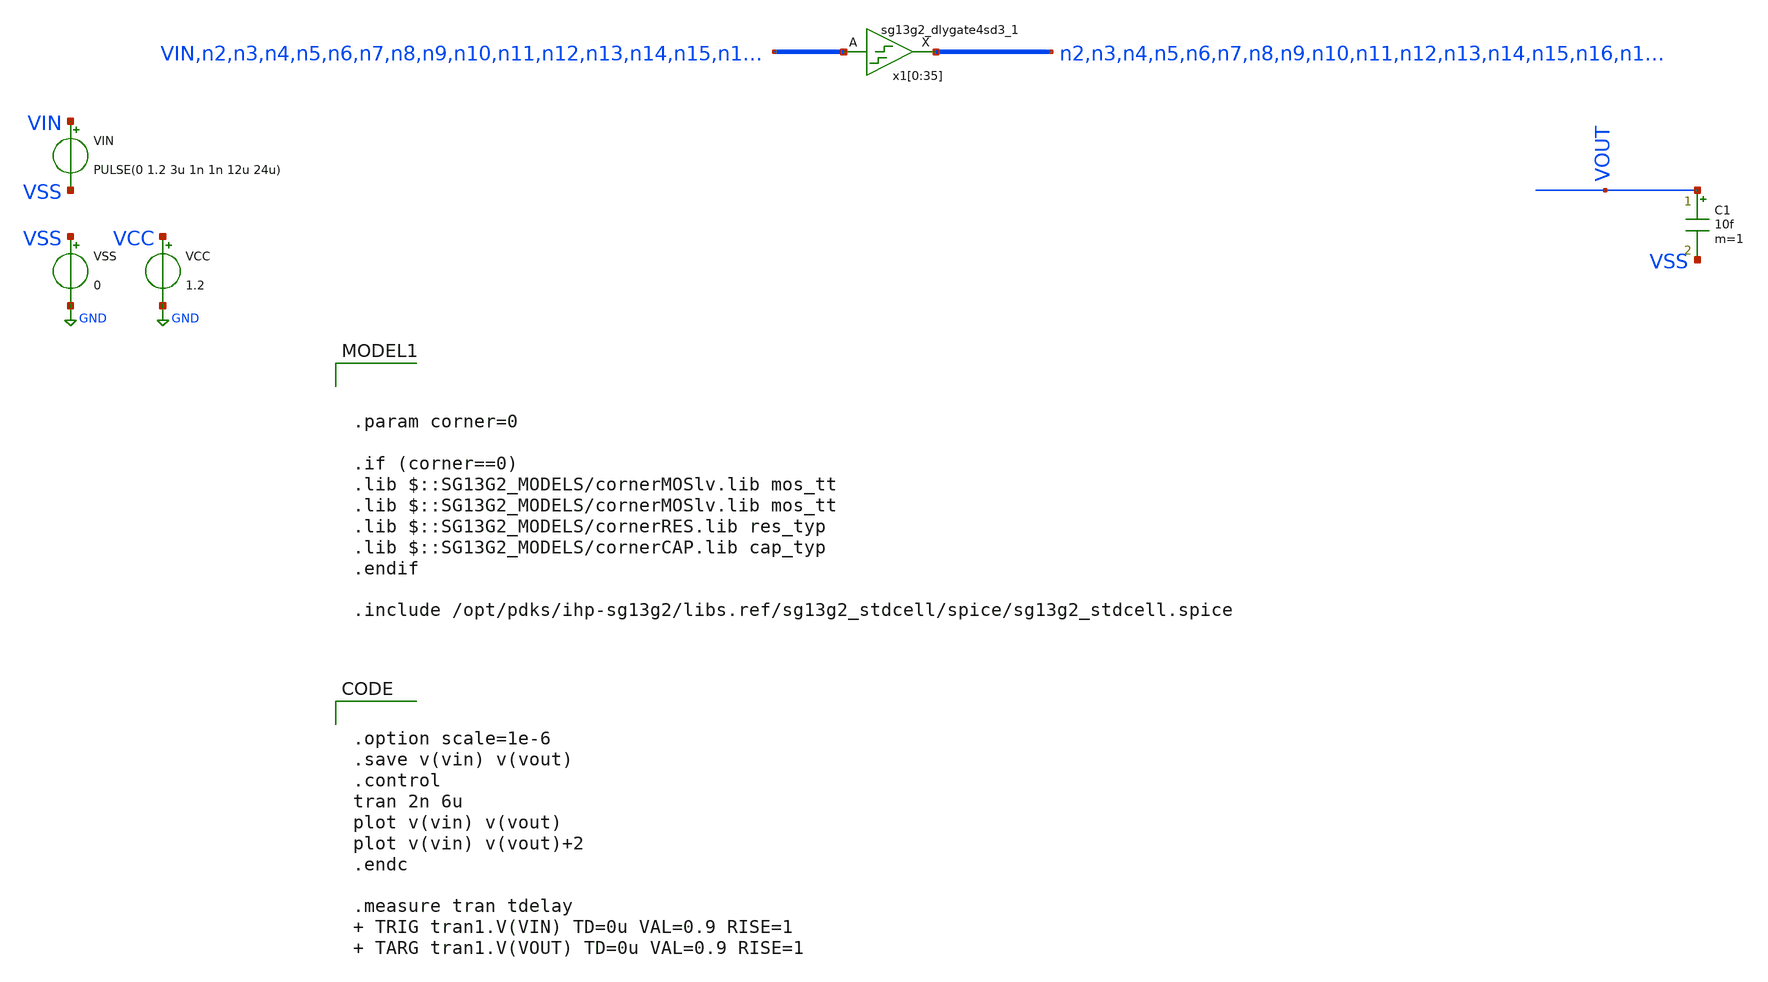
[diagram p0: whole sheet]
** sch_path: xschem/tb_largedelay_reportslack.sch
**.subckt tb_largedelay_reportslack
VCC VCC GND 1.2
VSS VSS GND 0
VIN VIN VSS PULSE(0 1.2 3u 1n 1n 12u 24u)
C1 VOUT VSS 10f m=1
x1[0] n2 VIN VCC VSS sg13g2_dlygate4sd3_1
x1[1] n3 n2 VCC VSS sg13g2_dlygate4sd3_1
x1[2] n4 n3 VCC VSS sg13g2_dlygate4sd3_1
x1[3] n5 n4 VCC VSS sg13g2_dlygate4sd3_1
x1[4] n6 n5 VCC VSS sg13g2_dlygate4sd3_1
x1[5] n7 n6 VCC VSS sg13g2_dlygate4sd3_1
x1[6] n8 n7 VCC VSS sg13g2_dlygate4sd3_1
x1[7] n9 n8 VCC VSS sg13g2_dlygate4sd3_1
x1[8] n10 n9 VCC VSS sg13g2_dlygate4sd3_1
x1[9] n11 n10 VCC VSS sg13g2_dlygate4sd3_1
x1[10] n12 n11 VCC VSS sg13g2_dlygate4sd3_1
x1[11] n13 n12 VCC VSS sg13g2_dlygate4sd3_1
x1[12] n14 n13 VCC VSS sg13g2_dlygate4sd3_1
x1[13] n15 n14 VCC VSS sg13g2_dlygate4sd3_1
x1[14] n16 n15 VCC VSS sg13g2_dlygate4sd3_1
x1[15] n17 n16 VCC VSS sg13g2_dlygate4sd3_1
x1[16] n18 n17 VCC VSS sg13g2_dlygate4sd3_1
x1[17] n19 n18 VCC VSS sg13g2_dlygate4sd3_1
x1[18] n20 n19 VCC VSS sg13g2_dlygate4sd3_1
x1[19] n21 n20 VCC VSS sg13g2_dlygate4sd3_1
x1[20] n22 n21 VCC VSS sg13g2_dlygate4sd3_1
x1[21] n23 n22 VCC VSS sg13g2_dlygate4sd3_1
x1[22] n24 n23 VCC VSS sg13g2_dlygate4sd3_1
x1[23] n25 n24 VCC VSS sg13g2_dlygate4sd3_1
x1[24] n26 n25 VCC VSS sg13g2_dlygate4sd3_1
x1[25] n27 n26 VCC VSS sg13g2_dlygate4sd3_1
x1[26] n28 n27 VCC VSS sg13g2_dlygate4sd3_1
x1[27] n29 n28 VCC VSS sg13g2_dlygate4sd3_1
x1[28] n30 n29 VCC VSS sg13g2_dlygate4sd3_1
x1[29] n31 n30 VCC VSS sg13g2_dlygate4sd3_1
x1[30] n32 n31 VCC VSS sg13g2_dlygate4sd3_1
x1[31] n33 n32 VCC VSS sg13g2_dlygate4sd3_1
x1[32] n34 n33 VCC VSS sg13g2_dlygate4sd3_1
x1[33] n35 n34 VCC VSS sg13g2_dlygate4sd3_1
x1[34] n36 n35 VCC VSS sg13g2_dlygate4sd3_1
x1[35] VOUT n36 VCC VSS sg13g2_dlygate4sd3_1
**** begin user architecture code


.option scale=1e-6
.save v(vin) v(vout)
.control
tran 2n 6u
plot v(vin) v(vout)
plot v(vin) v(vout)+2
.endc

.measure tran tdelay  TRIG tran1.V(VIN) TD=0u VAL=0.9 RISE=1  TARG tran1.V(VOUT) TD=0u VAL=0.9
+ RISE=1






.param corner=0

.if (corner==0)
.lib $::SG13G2_MODELS/cornerMOSlv.lib mos_tt
.lib $::SG13G2_MODELS/cornerMOSlv.lib mos_tt
.lib $::SG13G2_MODELS/cornerRES.lib res_typ
.lib $::SG13G2_MODELS/cornerCAP.lib cap_typ
.endif

.include /opt/pdks/ihp-sg13g2/libs.ref/sg13g2_stdcell/spice/sg13g2_stdcell.spice

**** end user architecture code
**.ends

* expanding   symbol:  sg13g2_stdcells/sg13g2_dlygate4sd3_1.sym # of pins=2
** sym_path: sg13g2_stdcells/sg13g2_dlygate4sd3_1.sym
** sch_path: sg13g2_stdcells/sg13g2_dlygate4sd3_1.sch
.subckt sg13g2_dlygate4sd3_1 X A VDD VSS
*.ipin A
*.opin X
*.iopin VDD
*.iopin VSS
XM1 net3 A VSS VSS sg13_lv_nmos w=420.00n l=130.00n ng=1 m=1 mm_ok=1
XM2 net1 net3 VSS VSS sg13_lv_nmos w=420.00n l=500.0n ng=1 m=1 mm_ok=1
XM3 net2 net1 VSS VSS sg13_lv_nmos w=420.00n l=500.0n ng=1 m=1 mm_ok=1
XM4 X net2 VSS VSS sg13_lv_nmos w=740.00n l=130.00n ng=1 m=1 mm_ok=1
XM5 net3 A VDD VDD sg13_lv_pmos w=420.00n l=130.00n ng=1 m=1 mm_ok=1
XM6 net1 net3 VDD VDD sg13_lv_pmos w=1.000u l=500.0n ng=1 m=1 mm_ok=1
XM7 net2 net1 VDD VDD sg13_lv_pmos w=1.000u l=500.0n ng=1 m=1 mm_ok=1
XM8 X net2 VDD VDD sg13_lv_pmos w=1.12u l=130.00n ng=1 m=1 mm_ok=1
.ends

.GLOBAL GND
.end
